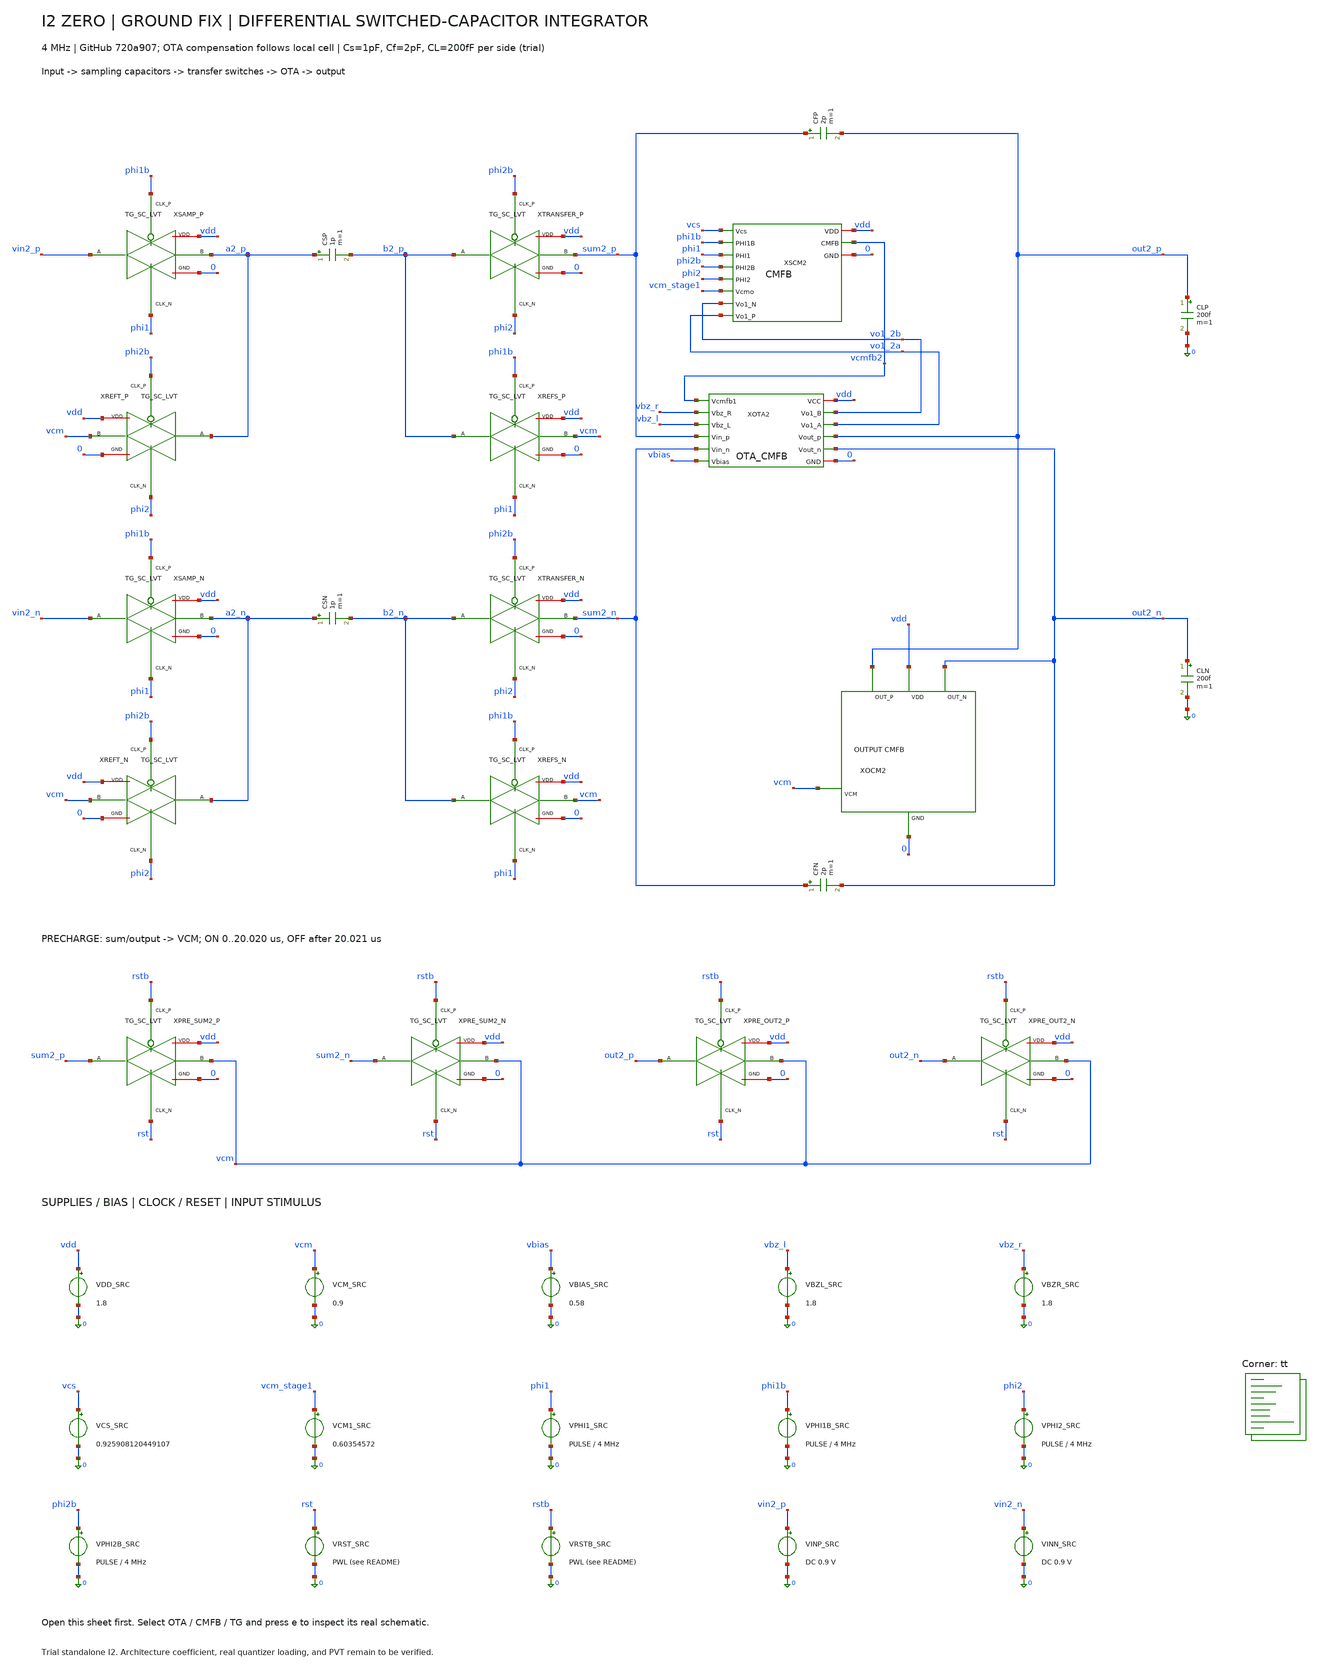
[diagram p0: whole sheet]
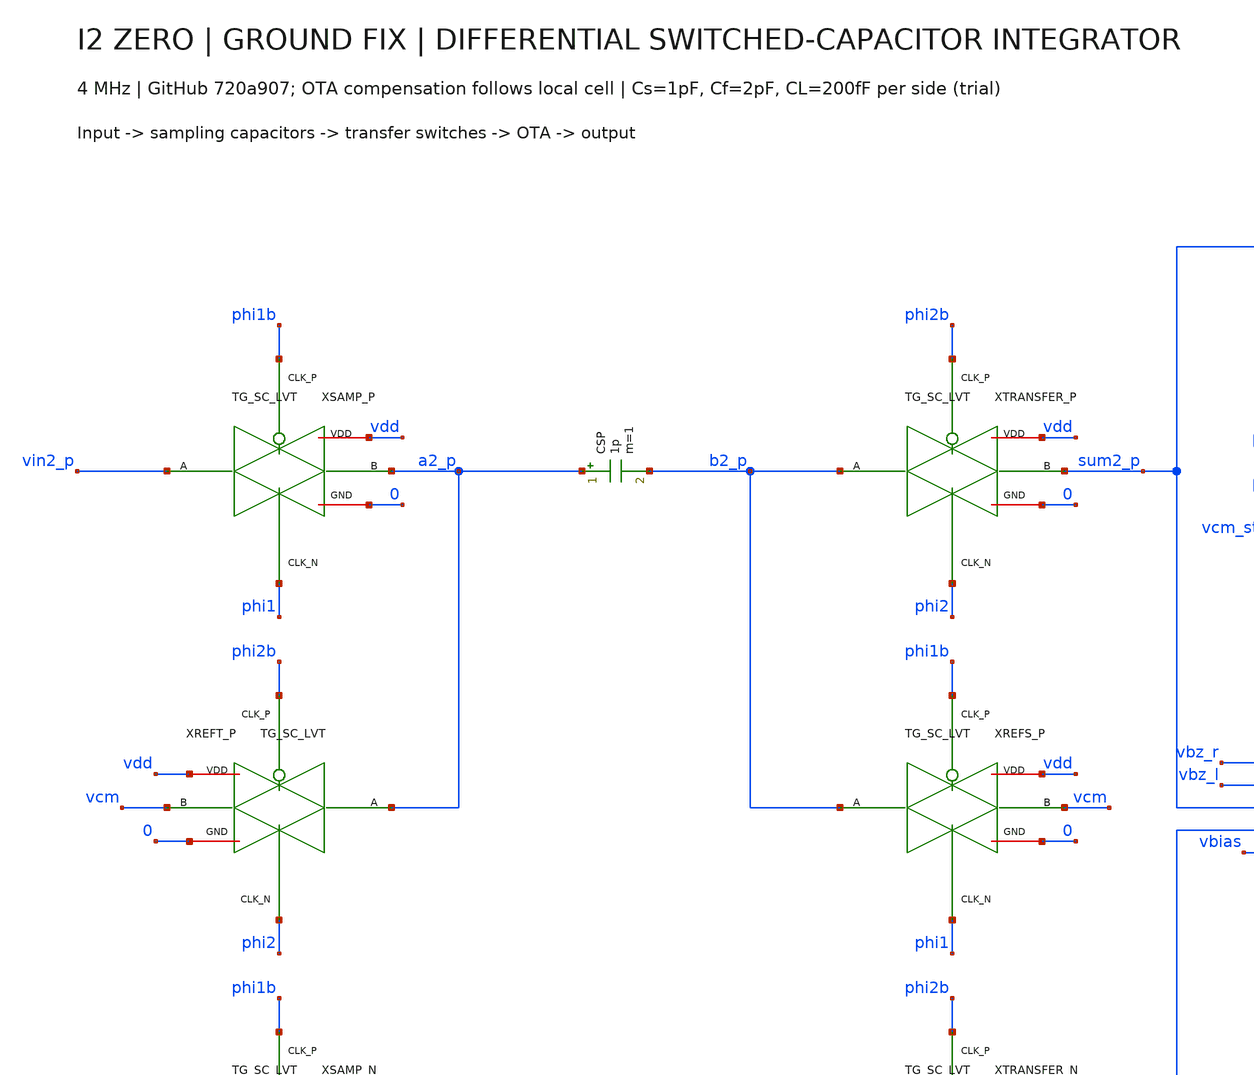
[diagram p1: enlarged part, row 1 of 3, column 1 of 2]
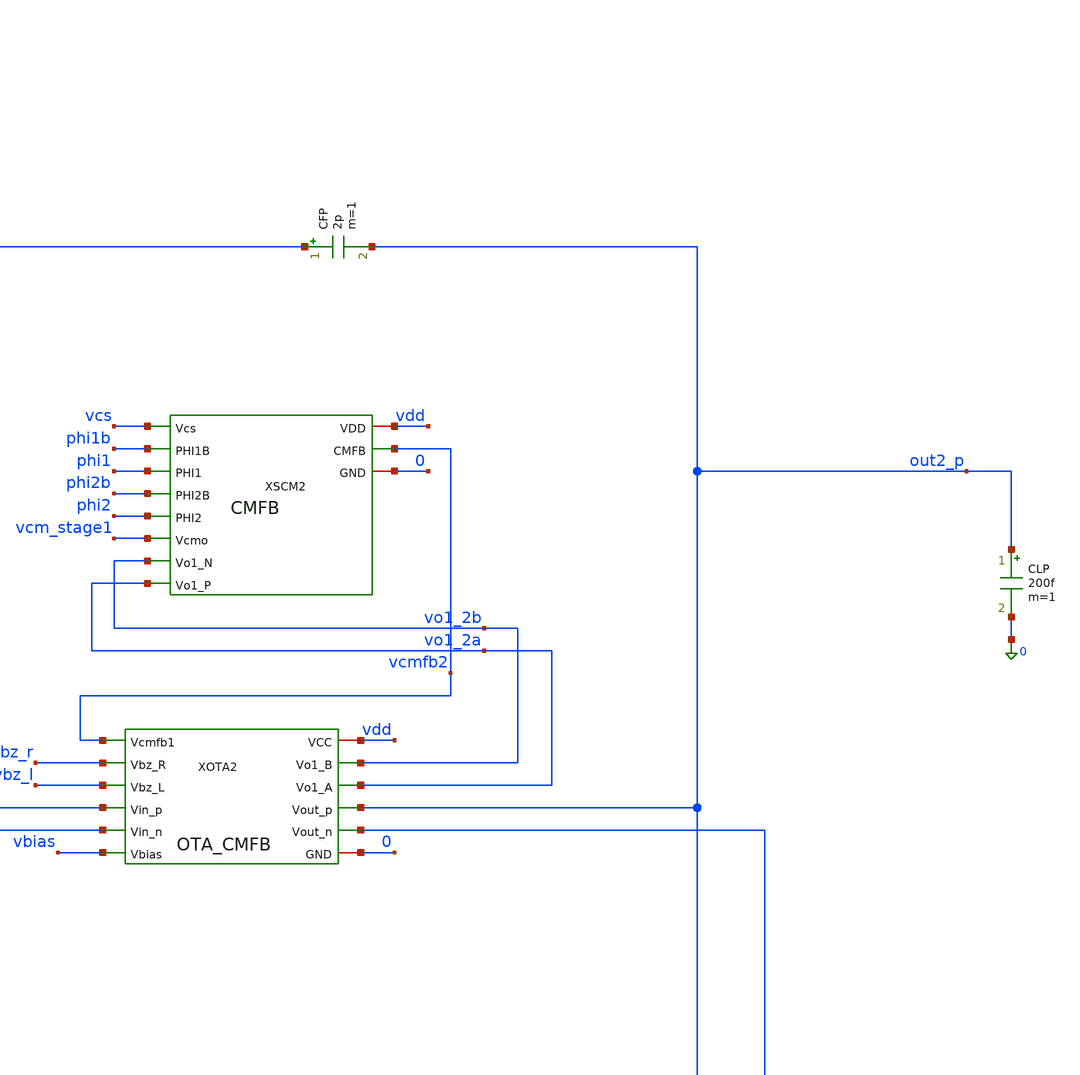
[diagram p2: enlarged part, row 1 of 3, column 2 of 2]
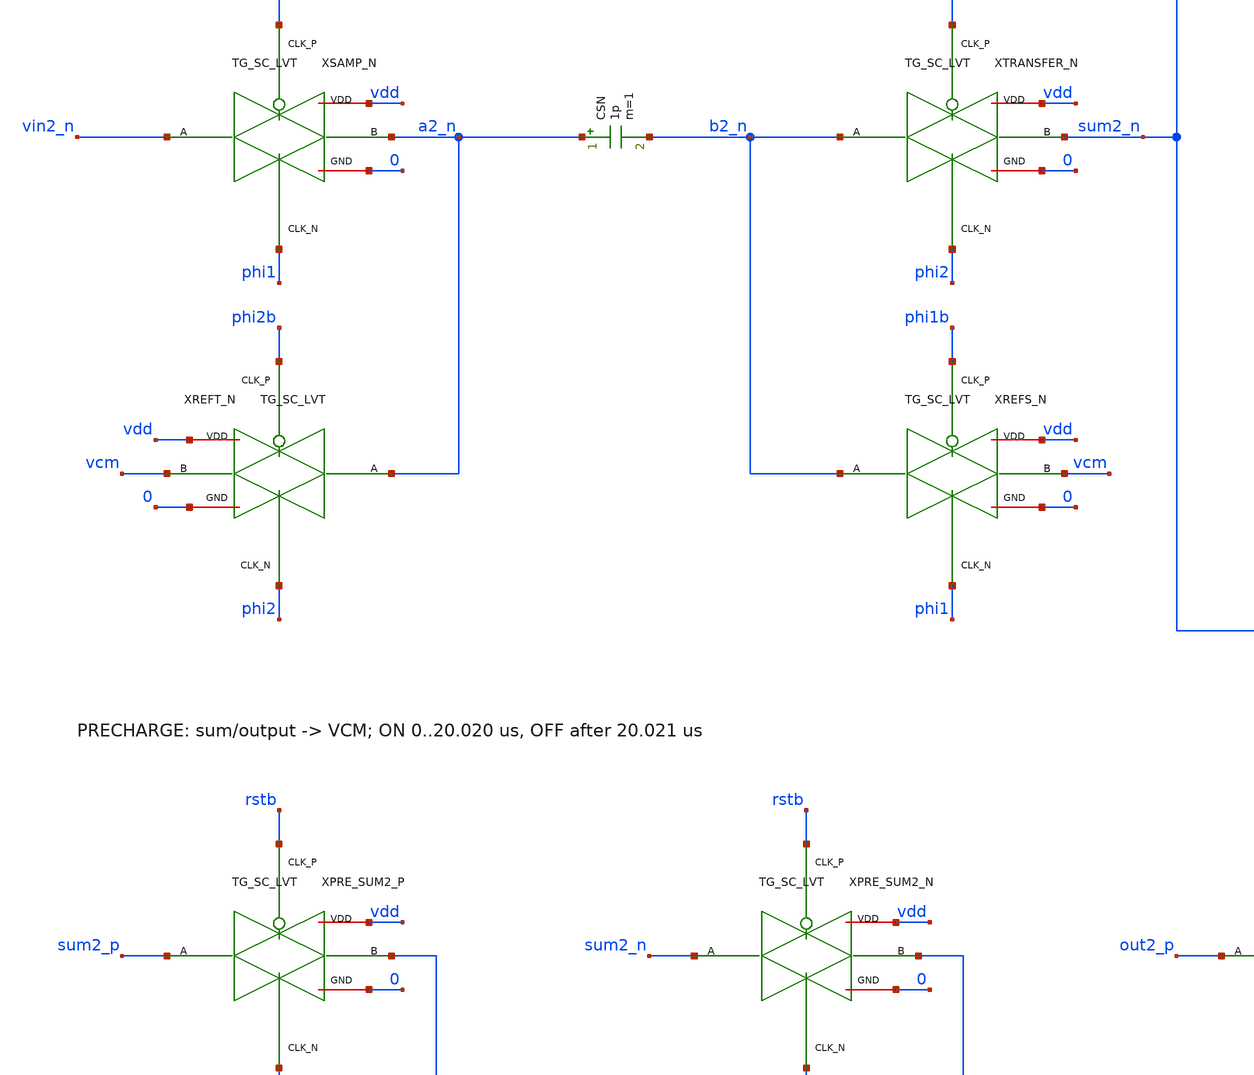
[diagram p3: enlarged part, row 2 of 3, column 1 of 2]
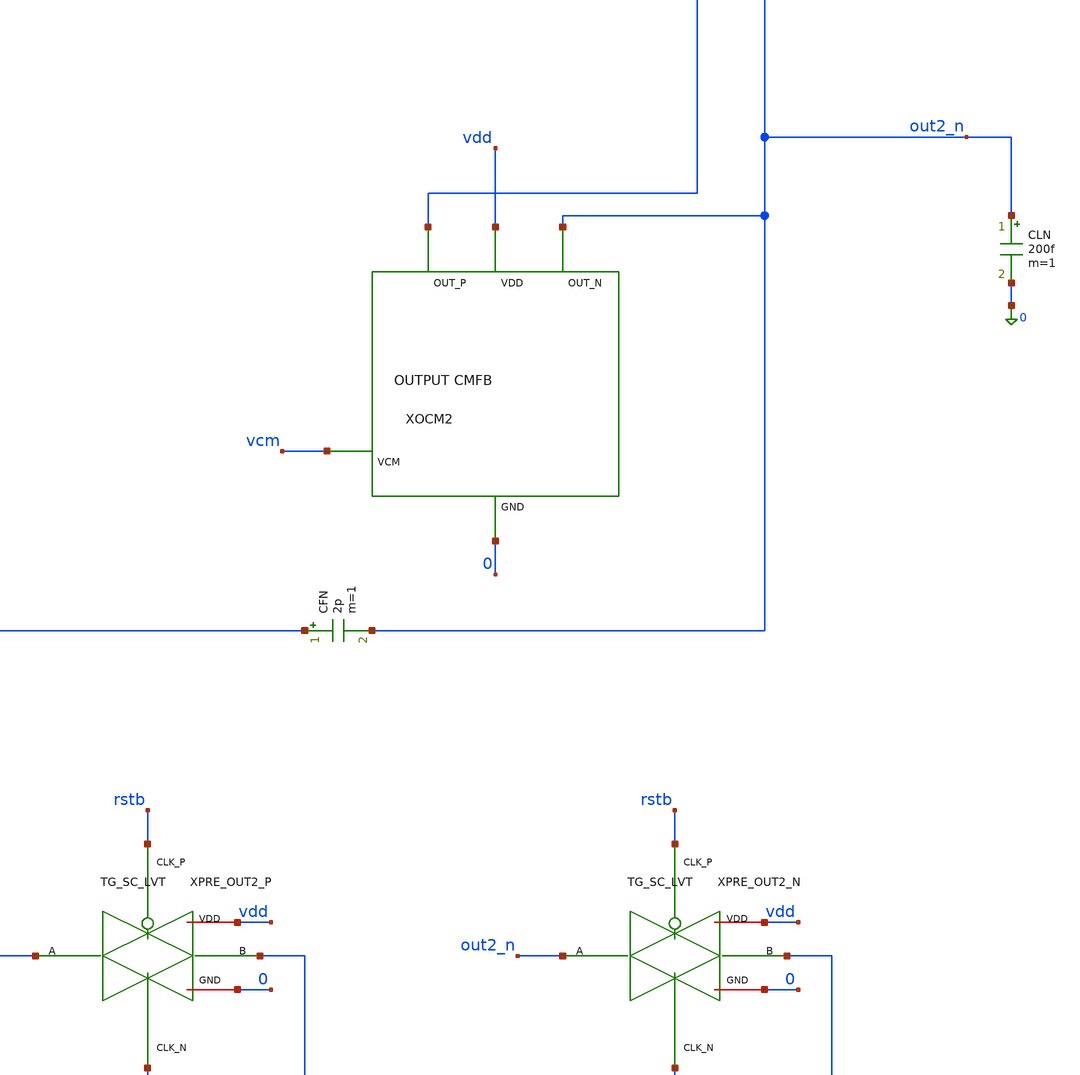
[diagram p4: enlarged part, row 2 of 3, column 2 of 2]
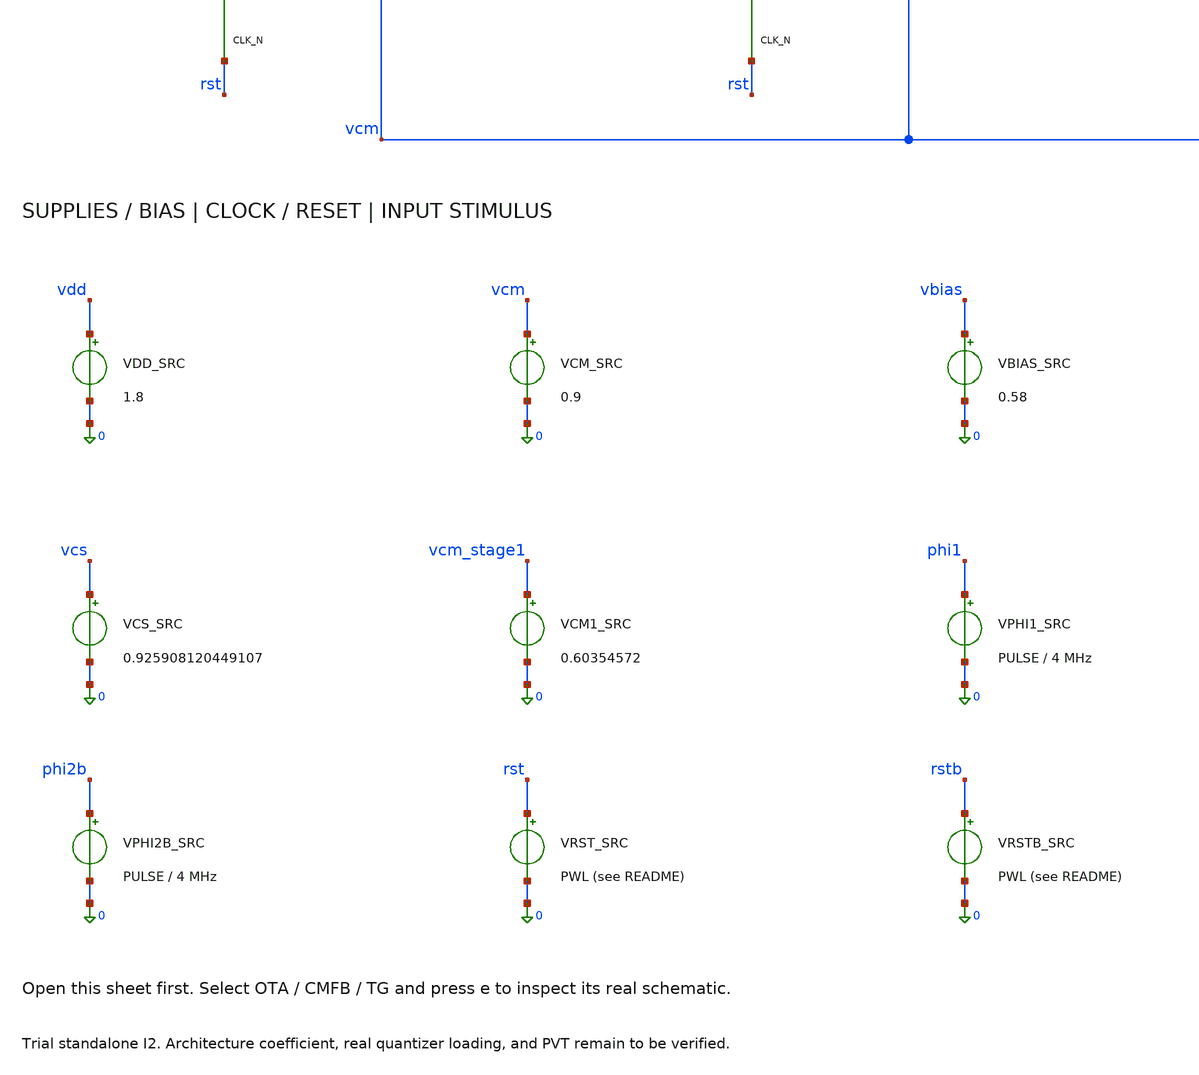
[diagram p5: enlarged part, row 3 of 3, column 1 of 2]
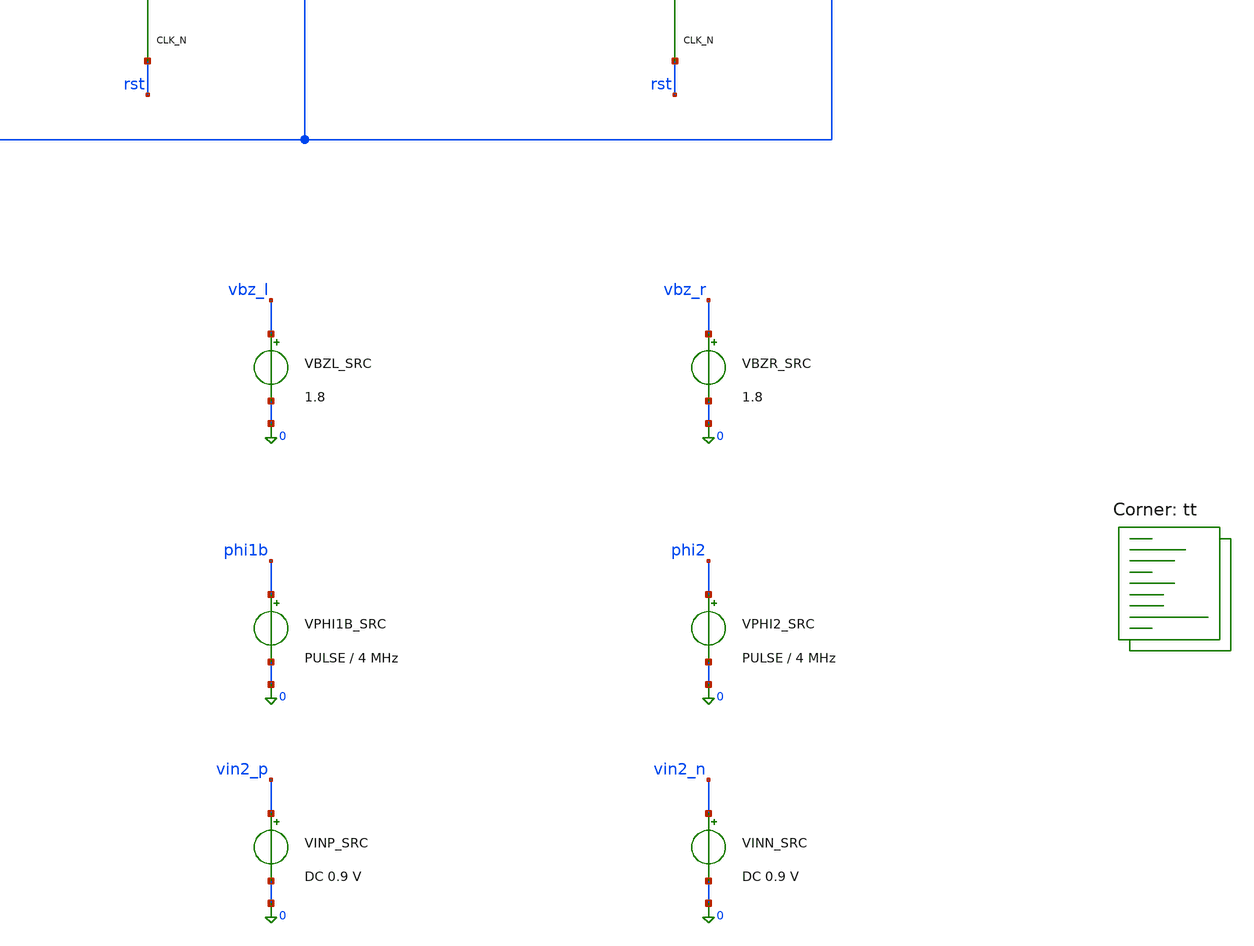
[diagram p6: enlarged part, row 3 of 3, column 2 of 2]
** sch_path: blocks/05_Switch_Network/sim/tb_I2_negative_groundfix.sch
**.subckt tb_I2_negative_groundfix
XSAMP_P vin2_p a2_p phi1b phi1 vdd 0 TG_SC_LVT
CSP a2_p b2_p 1p m=1
XTRANSFER_P b2_p sum2_p phi2b phi2 vdd 0 TG_SC_LVT
XREFT_P a2_p vcm phi2b phi2 vdd 0 TG_SC_LVT
XREFS_P b2_p vcm phi1b phi1 vdd 0 TG_SC_LVT
XSAMP_N vin2_n a2_n phi1b phi1 vdd 0 TG_SC_LVT
CSN a2_n b2_n 1p m=1
XTRANSFER_N b2_n sum2_n phi2b phi2 vdd 0 TG_SC_LVT
XREFT_N a2_n vcm phi2b phi2 vdd 0 TG_SC_LVT
XREFS_N b2_n vcm phi1b phi1 vdd 0 TG_SC_LVT
XOTA2 vdd vcmfb2 vbz_r vbz_l sum2_p sum2_n vo1_2b vo1_2a out2_p out2_n vbias 0 OTA_CMFB
CFP sum2_p out2_p 2p m=1
CFN sum2_n out2_n 2p m=1
CLP out2_p 0 200f m=1
CLN out2_n 0 200f m=1
XSCM2 vcmfb2 vcs phi1b phi1 vdd phi2b 0 phi2 vcm_stage1 vo1_2b vo1_2a CMFB
XOCM2 vdd 0 out2_p out2_n vcm CMFB_OUT_I2_Wired
XPRE_SUM2_P sum2_p vcm rstb rst vdd 0 TG_SC_LVT
XPRE_SUM2_N sum2_n vcm rstb rst vdd 0 TG_SC_LVT
XPRE_OUT2_P out2_p vcm rstb rst vdd 0 TG_SC_LVT
XPRE_OUT2_N out2_n vcm rstb rst vdd 0 TG_SC_LVT
VDD_SRC vdd 0 1.8
VCM_SRC vcm 0 0.9
VBIAS_SRC vbias 0 0.58
VBZL_SRC vbz_l 0 1.8
VBZR_SRC vbz_r 0 1.8
VCS_SRC vcs 0 0.925908120449107
VCM1_SRC vcm_stage1 0 0.60354572
VPHI1_SRC phi1 0 PULSE(0 1.8 30n 1n 1n 110n 250n)
VPHI1B_SRC phi1b 0 PULSE(1.8 0 30n 1n 1n 110n 250n)
VPHI2_SRC phi2 0 PULSE(0 1.8 155n 1n 1n 110n 250n)
VPHI2B_SRC phi2b 0 PULSE(1.8 0 155n 1n 1n 110n 250n)
VRST_SRC rst 0 PWL(0 1.8 20.020u 1.8 20.021u 0 30u 0)
VRSTB_SRC rstb 0 PWL(0 0 20.020u 0 20.021u 1.8 30u 1.8)
VINP_SRC vin2_p 0 PWL(0 0.9 22.005u 0.9 22.006u 0.895 24.005u 0.895 24.006u 0.9 30u 0.9)
VINN_SRC vin2_n 0 PWL(0 0.9 22.005u 0.9 22.006u 0.905 24.005u 0.905 24.006u 0.9 30u 0.9)
**** begin user architecture code


* GitHub 720a907: OTA C1/C2 MF=1000; no device sizes modified.
* Trial characterization values only. Set from architecture before I2 signoff.
.param CS2_TEST=1p CF2_TEST=2p CL2_TEST=200f I2_ARCH_CONFIRMED=0
.option scale=1e-6 reltol=1e-5 abstol=1e-14 vntol=1e-8
.temp 27
.control
save all
set wr_singlescale
set wr_vecnames
set numdgt=15
tran 200p 30u 0 100p
let vd2=v(OUT2_P)-v(OUT2_N)
let cm2=(v(OUT2_P)+v(OUT2_N))/2
let cmfirst2=(v(VO1_2A)+v(VO1_2B))/2
meas tran VDD_END FIND v(vdd) AT=29.99u
meas tran VINP_END FIND v(vin2_p) AT=29.99u
meas tran VINN_END FIND v(vin2_n) AT=29.99u
meas tran RST_END FIND v(rst) AT=29.99u
meas tran PHI1_MIN MIN v(phi1) FROM=29u TO=30u
meas tran PHI1_MAX MAX v(phi1) FROM=29u TO=30u
meas tran VD_BEFORE FIND vd2 AT=22.014u
meas tran VD_CYCLE8 FIND vd2 AT=24.014u
meas tran VD_CYCLE24 FIND vd2 AT=28.014u
meas tran CM_END AVG cm2 FROM=29u TO=30u
meas tran CM_FIRST_END AVG cmfirst2 FROM=29u TO=30u
meas tran CM_MIN MIN cm2 FROM=21u TO=30u
meas tran CM_MAX MAX cm2 FROM=21u TO=30u
meas tran DIFF_MIN MIN vd2 FROM=21u TO=30u
meas tran DIFF_MAX MAX vd2 FROM=21u TO=30u
let burst_delta=VD_CYCLE8-VD_BEFORE
let hold_drift=VD_CYCLE24-VD_CYCLE8
print burst_delta hold_drift
wrdata waveform_I2_negative_groundfix.dat v(VIN2_P) v(VIN2_N) v(SUM2_P) v(SUM2_N) v(OUT2_P)
+ v(OUT2_N) v(VO1_2A) v(VO1_2B) v(VCMFB2) v(PHI1) v(PHI2) v(RST) i(VDD_SRC) v(vdd) v(vcm) v(phi1b) v(phi2b)
+ v(rstb)
echo I2_TRIAL_ONLY_NO_ARCHITECTURE_OR_PVT_PASS
plot v(OUT2_P) v(OUT2_N) cm2
plot vd2
.endc


.lib $::SKYWATER_MODELS/sky130.lib.spice tt
**** end user architecture code
**.ends
.end
